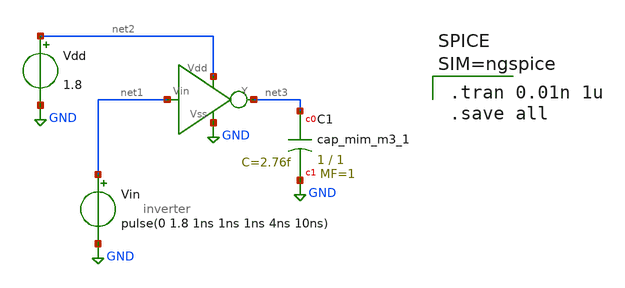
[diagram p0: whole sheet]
** sch_path: exp/inverter_hierarchical/inverter_hierarchical.sch
**.subckt inverter_hierarchical
Vdd net2 GND 1.8
Vin net1 GND pulse(0 1.8 1ns 1ns 1ns 4ns 10ns)
XC1 net3 GND sky130_fd_pr__cap_mim_m3_1 W=1 L=1 MF=1 m=1
x1 GND net1 net2 net3 inverter
**** begin user architecture code


.tran 0.01n 1u
.save all



** opencircuitdesign pdks install
.lib $::SKYWATER_MODELS/sky130.lib.spice tt


**** end user architecture code
**.ends
.GLOBAL GND
.end
